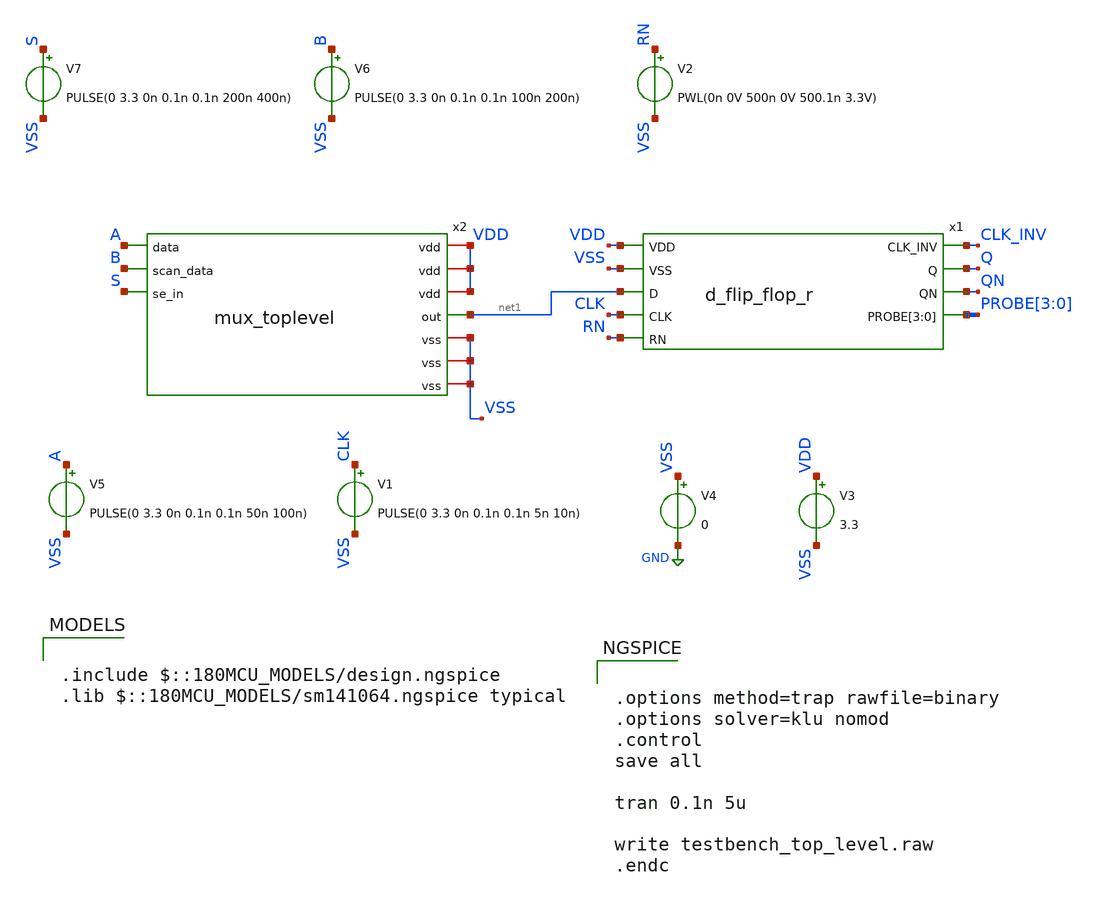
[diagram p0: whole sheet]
** sch_path: designs/schematics/testbench_top_level_mux_tg.sch
**.subckt testbench_top_level_mux_tg
V1 CLK VSS PULSE(0 3.3 0n 0.1n 0.1n 5n 10n)
V3 VDD VSS 3.3
V4 VSS GND 0
V5 A VSS PULSE(0 3.3 0n 0.1n 0.1n 50n 100n)
V6 B VSS PULSE(0 3.3 0n 0.1n 0.1n 100n 200n)
V7 S VSS PULSE(0 3.3 0n 0.1n 0.1n 200n 400n)
V2 RN VSS PWL(0n 0V 500n 0V 500.1n 3.3V)
x1 VDD CLK_INV VSS Q net1 QN CLK PROBE[3] PROBE[2] PROBE[1] PROBE[0] RN d_flip_flop_r
x2 VDD A VSS net1 B S mux_toplevel
**** begin user architecture code

.include $::180MCU_MODELS/design.ngspice
.lib $::180MCU_MODELS/sm141064.ngspice typical



.options method=trap rawfile=binary
.options solver=klu nomod
.control
save all

tran 0.1n 5u

write testbench_top_level.raw
.endc


**** end user architecture code
**.ends

* expanding   symbol:  voidwalkers-scandff-gf180mcu/designs/schematics/d_flip_flop/d_flip_flop_r.sym
*+ # of pins=9
** sym_path: designs/schematics/d_flip_flop/d_flip_flop_r.sym
** sch_path: designs/schematics/d_flip_flop/d_flip_flop_r.sch
.subckt d_flip_flop_r VDD CLK_INV VSS Q D QN CLK PROBE[3] PROBE[2] PROBE[1] PROBE[0] RN
*.ipin D
*.ipin VDD
*.ipin VSS
*.opin Q
*.ipin CLK
*.ipin RN
*.opin CLK_INV
*.opin QN
*.opin PROBE[3],PROBE[2],PROBE[1],PROBE[0]
XM1 net1 D VDD VDD pfet_03v3 L=0.3u W=1.7u nf=1 ad='int((nf+1)/2) * W/nf * 0.18u' as='int((nf+2)/2) * W/nf * 0.18u'
+ pd='2*int((nf+1)/2) * (W/nf + 0.18u)' ps='2*int((nf+2)/2) * (W/nf + 0.18u)' nrd='0.18u / W' nrs='0.18u / W'
+ sa=0 sb=0 sd=0 m=1
XM2 PROBE[0] CLK_INV net2 VSS nfet_03v3 L=0.3u W=0.85u nf=1 ad='int((nf+1)/2) * W/nf * 0.18u' as='int((nf+2)/2) * W/nf * 0.18u'
+ pd='2*int((nf+1)/2) * (W/nf + 0.18u)' ps='2*int((nf+2)/2) * (W/nf + 0.18u)' nrd='0.18u / W' nrs='0.18u / W'
+ sa=0 sb=0 sd=0 m=1
XM3 PROBE[0] CLK net1 VDD pfet_03v3 L=0.3u W=1.7u nf=1 ad='int((nf+1)/2) * W/nf * 0.18u' as='int((nf+2)/2) * W/nf * 0.18u'
+ pd='2*int((nf+1)/2) * (W/nf + 0.18u)' ps='2*int((nf+2)/2) * (W/nf + 0.18u)' nrd='0.18u / W' nrs='0.18u / W'
+ sa=0 sb=0 sd=0 m=1
XM4 net2 D VSS VSS nfet_03v3 L=0.3u W=0.85u nf=1 ad='int((nf+1)/2) * W/nf * 0.18u' as='int((nf+2)/2) * W/nf * 0.18u'
+ pd='2*int((nf+1)/2) * (W/nf + 0.18u)' ps='2*int((nf+2)/2) * (W/nf + 0.18u)' nrd='0.18u / W' nrs='0.18u / W'
+ sa=0 sb=0 sd=0 m=1
XM5 CLK_INV CLK VDD VDD pfet_03v3 L=0.3u W=1.7u nf=1 ad='int((nf+1)/2) * W/nf * 0.18u' as='int((nf+2)/2) * W/nf * 0.18u'
+ pd='2*int((nf+1)/2) * (W/nf + 0.18u)' ps='2*int((nf+2)/2) * (W/nf + 0.18u)' nrd='0.18u / W' nrs='0.18u / W'
+ sa=0 sb=0 sd=0 m=1
XM8 CLK_INV CLK VSS VSS nfet_03v3 L=0.3u W=0.85u nf=1 ad='int((nf+1)/2) * W/nf * 0.18u' as='int((nf+2)/2) * W/nf * 0.18u'
+ pd='2*int((nf+1)/2) * (W/nf + 0.18u)' ps='2*int((nf+2)/2) * (W/nf + 0.18u)' nrd='0.18u / W' nrs='0.18u / W'
+ sa=0 sb=0 sd=0 m=1
XM13 net3 PROBE[1] VDD VDD pfet_03v3 L=0.3u W=1.7u nf=1 ad='int((nf+1)/2) * W/nf * 0.18u' as='int((nf+2)/2) * W/nf * 0.18u'
+ pd='2*int((nf+1)/2) * (W/nf + 0.18u)' ps='2*int((nf+2)/2) * (W/nf + 0.18u)' nrd='0.18u / W' nrs='0.18u / W'
+ sa=0 sb=0 sd=0 m=1
XM14 PROBE[0] CLK net4 VSS nfet_03v3 L=0.3u W=0.85u nf=1 ad='int((nf+1)/2) * W/nf * 0.18u' as='int((nf+2)/2) * W/nf * 0.18u'
+ pd='2*int((nf+1)/2) * (W/nf + 0.18u)' ps='2*int((nf+2)/2) * (W/nf + 0.18u)' nrd='0.18u / W' nrs='0.18u / W'
+ sa=0 sb=0 sd=0 m=1
XM15 PROBE[0] CLK_INV net3 VDD pfet_03v3 L=0.3u W=1.7u nf=1 ad='int((nf+1)/2) * W/nf * 0.18u' as='int((nf+2)/2) * W/nf * 0.18u'
+ pd='2*int((nf+1)/2) * (W/nf + 0.18u)' ps='2*int((nf+2)/2) * (W/nf + 0.18u)' nrd='0.18u / W' nrs='0.18u / W'
+ sa=0 sb=0 sd=0 m=1
XM16 net4 PROBE[1] VSS VSS nfet_03v3 L=0.3u W=0.85u nf=1 ad='int((nf+1)/2) * W/nf * 0.18u' as='int((nf+2)/2) * W/nf * 0.18u'
+ pd='2*int((nf+1)/2) * (W/nf + 0.18u)' ps='2*int((nf+2)/2) * (W/nf + 0.18u)' nrd='0.18u / W' nrs='0.18u / W'
+ sa=0 sb=0 sd=0 m=1
XM9 net5 PROBE[1] VDD VDD pfet_03v3 L=0.3u W=1.7u nf=1 ad='int((nf+1)/2) * W/nf * 0.18u' as='int((nf+2)/2) * W/nf * 0.18u'
+ pd='2*int((nf+1)/2) * (W/nf + 0.18u)' ps='2*int((nf+2)/2) * (W/nf + 0.18u)' nrd='0.18u / W' nrs='0.18u / W'
+ sa=0 sb=0 sd=0 m=1
XM10 PROBE[2] CLK net6 VSS nfet_03v3 L=0.3u W=0.85u nf=1 ad='int((nf+1)/2) * W/nf * 0.18u' as='int((nf+2)/2) * W/nf * 0.18u'
+ pd='2*int((nf+1)/2) * (W/nf + 0.18u)' ps='2*int((nf+2)/2) * (W/nf + 0.18u)' nrd='0.18u / W' nrs='0.18u / W'
+ sa=0 sb=0 sd=0 m=1
XM11 PROBE[2] CLK_INV net5 VDD pfet_03v3 L=0.3u W=1.7u nf=1 ad='int((nf+1)/2) * W/nf * 0.18u' as='int((nf+2)/2) * W/nf * 0.18u'
+ pd='2*int((nf+1)/2) * (W/nf + 0.18u)' ps='2*int((nf+2)/2) * (W/nf + 0.18u)' nrd='0.18u / W' nrs='0.18u / W'
+ sa=0 sb=0 sd=0 m=1
XM12 net6 PROBE[1] VSS VSS nfet_03v3 L=0.3u W=0.85u nf=1 ad='int((nf+1)/2) * W/nf * 0.18u' as='int((nf+2)/2) * W/nf * 0.18u'
+ pd='2*int((nf+1)/2) * (W/nf + 0.18u)' ps='2*int((nf+2)/2) * (W/nf + 0.18u)' nrd='0.18u / W' nrs='0.18u / W'
+ sa=0 sb=0 sd=0 m=1
XM19 net7 PROBE[3] VDD VDD pfet_03v3 L=0.3u W=1.7u nf=1 ad='int((nf+1)/2) * W/nf * 0.18u' as='int((nf+2)/2) * W/nf * 0.18u'
+ pd='2*int((nf+1)/2) * (W/nf + 0.18u)' ps='2*int((nf+2)/2) * (W/nf + 0.18u)' nrd='0.18u / W' nrs='0.18u / W'
+ sa=0 sb=0 sd=0 m=1
XM20 PROBE[2] CLK_INV net8 VSS nfet_03v3 L=0.3u W=0.85u nf=1 ad='int((nf+1)/2) * W/nf * 0.18u' as='int((nf+2)/2) * W/nf * 0.18u'
+ pd='2*int((nf+1)/2) * (W/nf + 0.18u)' ps='2*int((nf+2)/2) * (W/nf + 0.18u)' nrd='0.18u / W' nrs='0.18u / W'
+ sa=0 sb=0 sd=0 m=1
XM21 PROBE[2] CLK net7 VDD pfet_03v3 L=0.3u W=1.7u nf=1 ad='int((nf+1)/2) * W/nf * 0.18u' as='int((nf+2)/2) * W/nf * 0.18u'
+ pd='2*int((nf+1)/2) * (W/nf + 0.18u)' ps='2*int((nf+2)/2) * (W/nf + 0.18u)' nrd='0.18u / W' nrs='0.18u / W'
+ sa=0 sb=0 sd=0 m=1
XM22 net8 PROBE[3] VSS VSS nfet_03v3 L=0.3u W=0.85u nf=1 ad='int((nf+1)/2) * W/nf * 0.18u' as='int((nf+2)/2) * W/nf * 0.18u'
+ pd='2*int((nf+1)/2) * (W/nf + 0.18u)' ps='2*int((nf+2)/2) * (W/nf + 0.18u)' nrd='0.18u / W' nrs='0.18u / W'
+ sa=0 sb=0 sd=0 m=1
XM23 QN PROBE[3] VDD VDD pfet_03v3 L=0.3u W=1.7u nf=1 ad='int((nf+1)/2) * W/nf * 0.18u' as='int((nf+2)/2) * W/nf * 0.18u'
+ pd='2*int((nf+1)/2) * (W/nf + 0.18u)' ps='2*int((nf+2)/2) * (W/nf + 0.18u)' nrd='0.18u / W' nrs='0.18u / W'
+ sa=0 sb=0 sd=0 m=1
XM24 QN PROBE[3] VSS VSS nfet_03v3 L=0.3u W=0.85u nf=1 ad='int((nf+1)/2) * W/nf * 0.18u' as='int((nf+2)/2) * W/nf * 0.18u'
+ pd='2*int((nf+1)/2) * (W/nf + 0.18u)' ps='2*int((nf+2)/2) * (W/nf + 0.18u)' nrd='0.18u / W' nrs='0.18u / W'
+ sa=0 sb=0 sd=0 m=1
XM25 Q QN VDD VDD pfet_03v3 L=0.3u W=1.7u nf=1 ad='int((nf+1)/2) * W/nf * 0.18u' as='int((nf+2)/2) * W/nf * 0.18u'
+ pd='2*int((nf+1)/2) * (W/nf + 0.18u)' ps='2*int((nf+2)/2) * (W/nf + 0.18u)' nrd='0.18u / W' nrs='0.18u / W'
+ sa=0 sb=0 sd=0 m=1
XM26 Q QN VSS VSS nfet_03v3 L=0.3u W=0.85u nf=1 ad='int((nf+1)/2) * W/nf * 0.18u' as='int((nf+2)/2) * W/nf * 0.18u'
+ pd='2*int((nf+1)/2) * (W/nf + 0.18u)' ps='2*int((nf+2)/2) * (W/nf + 0.18u)' nrd='0.18u / W' nrs='0.18u / W'
+ sa=0 sb=0 sd=0 m=1
XM6 net9 PROBE[0] VDD VDD pfet_03v3 L=0.3u W=1.7u nf=1 ad='int((nf+1)/2) * W/nf * 0.18u' as='int((nf+2)/2) * W/nf * 0.18u'
+ pd='2*int((nf+1)/2) * (W/nf + 0.18u)' ps='2*int((nf+2)/2) * (W/nf + 0.18u)' nrd='0.18u / W' nrs='0.18u / W'
+ sa=0 sb=0 sd=0 m=1
XM27 PROBE[1] RN net9 VDD pfet_03v3 L=0.3u W=1.7u nf=1 ad='int((nf+1)/2) * W/nf * 0.18u' as='int((nf+2)/2) * W/nf * 0.18u'
+ pd='2*int((nf+1)/2) * (W/nf + 0.18u)' ps='2*int((nf+2)/2) * (W/nf + 0.18u)' nrd='0.18u / W' nrs='0.18u / W'
+ sa=0 sb=0 sd=0 m=1
XM28 PROBE[1] PROBE[0] VSS VSS nfet_03v3 L=0.3u W=0.85u nf=1 ad='int((nf+1)/2) * W/nf * 0.18u' as='int((nf+2)/2) * W/nf * 0.18u'
+ pd='2*int((nf+1)/2) * (W/nf + 0.18u)' ps='2*int((nf+2)/2) * (W/nf + 0.18u)' nrd='0.18u / W' nrs='0.18u / W'
+ sa=0 sb=0 sd=0 m=1
XM17 net10 PROBE[2] VDD VDD pfet_03v3 L=0.3u W=1.7u nf=1 ad='int((nf+1)/2) * W/nf * 0.18u' as='int((nf+2)/2) * W/nf * 0.18u'
+ pd='2*int((nf+1)/2) * (W/nf + 0.18u)' ps='2*int((nf+2)/2) * (W/nf + 0.18u)' nrd='0.18u / W' nrs='0.18u / W'
+ sa=0 sb=0 sd=0 m=1
XM29 PROBE[3] RN net10 VDD pfet_03v3 L=0.3u W=1.7u nf=1 ad='int((nf+1)/2) * W/nf * 0.18u' as='int((nf+2)/2) * W/nf * 0.18u'
+ pd='2*int((nf+1)/2) * (W/nf + 0.18u)' ps='2*int((nf+2)/2) * (W/nf + 0.18u)' nrd='0.18u / W' nrs='0.18u / W'
+ sa=0 sb=0 sd=0 m=1
XM30 PROBE[3] PROBE[2] VSS VSS nfet_03v3 L=0.3u W=0.85u nf=1 ad='int((nf+1)/2) * W/nf * 0.18u' as='int((nf+2)/2) * W/nf * 0.18u'
+ pd='2*int((nf+1)/2) * (W/nf + 0.18u)' ps='2*int((nf+2)/2) * (W/nf + 0.18u)' nrd='0.18u / W' nrs='0.18u / W'
+ sa=0 sb=0 sd=0 m=1
XM7 PROBE[1] RN VSS VSS nfet_03v3 L=0.3u W=0.85u nf=1 ad='int((nf+1)/2) * W/nf * 0.18u' as='int((nf+2)/2) * W/nf * 0.18u'
+ pd='2*int((nf+1)/2) * (W/nf + 0.18u)' ps='2*int((nf+2)/2) * (W/nf + 0.18u)' nrd='0.18u / W' nrs='0.18u / W'
+ sa=0 sb=0 sd=0 m=1
XM18 PROBE[3] RN VSS VSS nfet_03v3 L=0.3u W=0.85u nf=1 ad='int((nf+1)/2) * W/nf * 0.18u' as='int((nf+2)/2) * W/nf * 0.18u'
+ pd='2*int((nf+1)/2) * (W/nf + 0.18u)' ps='2*int((nf+2)/2) * (W/nf + 0.18u)' nrd='0.18u / W' nrs='0.18u / W'
+ sa=0 sb=0 sd=0 m=1
.ends


* expanding   symbol:
*+  voidwalkers-scandff-gf180mcu/designs/schematics/mux2x1_transmission_gate/mux_toplevel.sym # of pins=10
** sym_path: designs/schematics/mux2x1_transmission_gate/mux_toplevel.sym
** sch_path: designs/schematics/mux2x1_transmission_gate/mux_toplevel.sch
.subckt mux_toplevel vdd data vss out scan_data se_in
*.iopin vdd
*.opin out
*.ipin data
*.ipin scan_data
*.ipin se_in
*.iopin vdd
*.iopin vss
*.iopin vss
*.iopin vdd
*.iopin vss
x1 vdd se_in net1 vss mux_ctrl_logic
x2 vdd net1 data out se_in vss mux_tg
x3 vdd se_in scan_data out net1 vss mux_tg
.ends


* expanding   symbol:  mux_transmission_gate/mux_ctrl_logic.sym # of pins=4
** sym_path: designs/schematics/mux2x1_transmission_gate/mux_ctrl_logic.sym
** sch_path: designs/schematics/mux2x1_transmission_gate/mux_ctrl_logic.sch
.subckt mux_ctrl_logic vdd in out_inv gnd
*.iopin vdd
*.iopin gnd
*.iopin out_inv
*.iopin in
XM1 out_inv in gnd gnd nfet_03v3 L=0.28u W=0.22u nf=1 ad='int((nf+1)/2) * W/nf * 0.18u' as='int((nf+2)/2) * W/nf * 0.18u'
+ pd='2*int((nf+1)/2) * (W/nf + 0.18u)' ps='2*int((nf+2)/2) * (W/nf + 0.18u)' nrd='0.18u / W' nrs='0.18u / W'
+ sa=0 sb=0 sd=0 m=1
XM2 out_inv in vdd vdd pfet_03v3 L=0.28u W=0.22u nf=1 ad='int((nf+1)/2) * W/nf * 0.18u' as='int((nf+2)/2) * W/nf * 0.18u'
+ pd='2*int((nf+1)/2) * (W/nf + 0.18u)' ps='2*int((nf+2)/2) * (W/nf + 0.18u)' nrd='0.18u / W' nrs='0.18u / W'
+ sa=0 sb=0 sd=0 m=1
.ends


* expanding   symbol:  mux_transmission_gate/mux_tg.sym # of pins=6
** sym_path: designs/schematics/mux2x1_transmission_gate/mux_tg.sym
** sch_path: designs/schematics/mux2x1_transmission_gate/mux_tg.sch
.subckt mux_tg vdd pfet_gate in out nfet_gate gnd
*.iopin vdd
*.iopin gnd
*.iopin out
*.iopin in
*.iopin pfet_gate
*.iopin nfet_gate
XM1 in nfet_gate out gnd nfet_03v3 L=0.28u W=0.22u nf=1 ad='int((nf+1)/2) * W/nf * 0.18u' as='int((nf+2)/2) * W/nf * 0.18u'
+ pd='2*int((nf+1)/2) * (W/nf + 0.18u)' ps='2*int((nf+2)/2) * (W/nf + 0.18u)' nrd='0.18u / W' nrs='0.18u / W'
+ sa=0 sb=0 sd=0 m=1
XM2 in pfet_gate out vdd pfet_03v3 L=0.28u W=0.22u nf=1 ad='int((nf+1)/2) * W/nf * 0.18u' as='int((nf+2)/2) * W/nf * 0.18u'
+ pd='2*int((nf+1)/2) * (W/nf + 0.18u)' ps='2*int((nf+2)/2) * (W/nf + 0.18u)' nrd='0.18u / W' nrs='0.18u / W'
+ sa=0 sb=0 sd=0 m=1
.ends

.GLOBAL GND
.end
